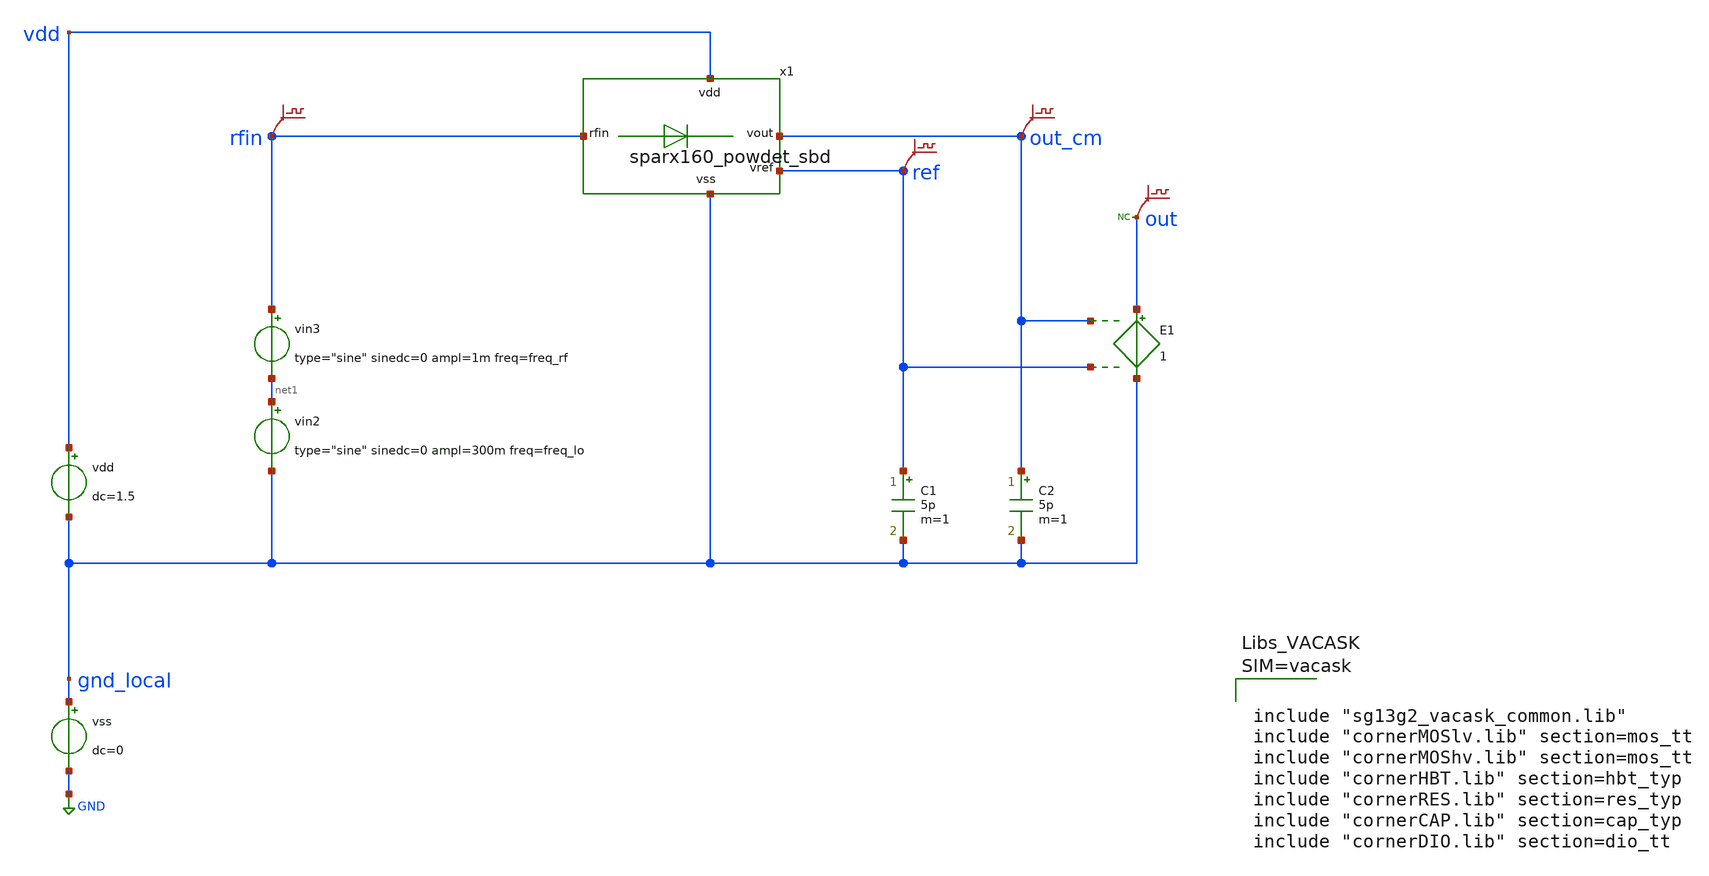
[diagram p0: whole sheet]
** sch_path: testbenches/powdet_sbd_tb_vacask.sch
* (c) 2026 Harald Pretl /// ICD@JKU
**.subckt powdet_sbd_tb_vacask
vss gnd_local GND dc=0
vdd vdd gnd_local dc=1.5
vin3 rfin net1 type="sine" sinedc=0 ampl=1m freq=freq_rf
.save v(rfin)
.save v(out_cm)
vin2 net1 gnd_local type="sine" sinedc=0 ampl=300m freq=freq_lo
.save v(ref)
C1 ref gnd_local 5p m=1
C2 out_cm gnd_local 5p m=1
E1 out gnd_local out_cm ref 1
.save v(out)
* noconn out
x1 out_cm ref vdd rfin gnd_local sparx160_powdet_sbd
**** begin user architecture code






**** end user architecture code
**.ends
.GLOBAL GND
.end
